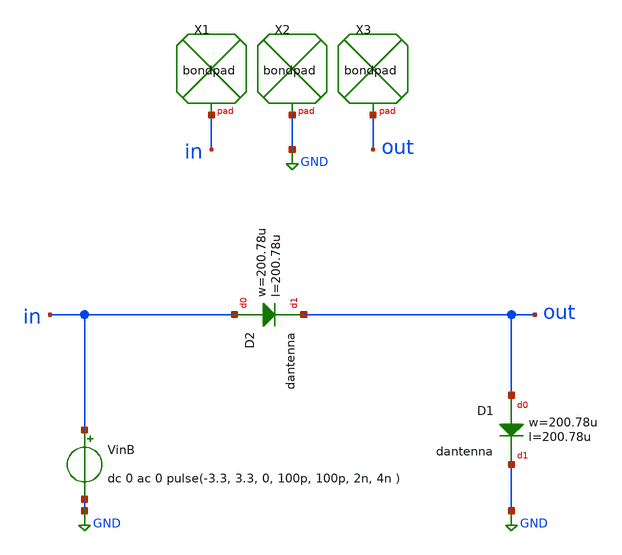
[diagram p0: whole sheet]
** sch_path: ihp-sg13g2/xschem_libs/sg13g2_tests_ase/tran_bondpad/schematic/tran_bondpad.sch
* Copyright 2023 IHP PDK Authors
**.subckt tran_bondpad
VinB in GND dc 0 ac 0 pulse(-3.3, 3.3, 0, 100p, 100p, 2n, 4n )
XD1 out GND dantenna l=200.78u w=200.78u
XD2 in out dantenna l=200.78u w=200.78u
XX1 in bondpad size=80u shape=0 padtype=0
XX2 GND bondpad size=80u shape=0 padtype=0
XX3 out bondpad size=80u shape=0 padtype=0
**.ends
.GLOBAL GND
.end
